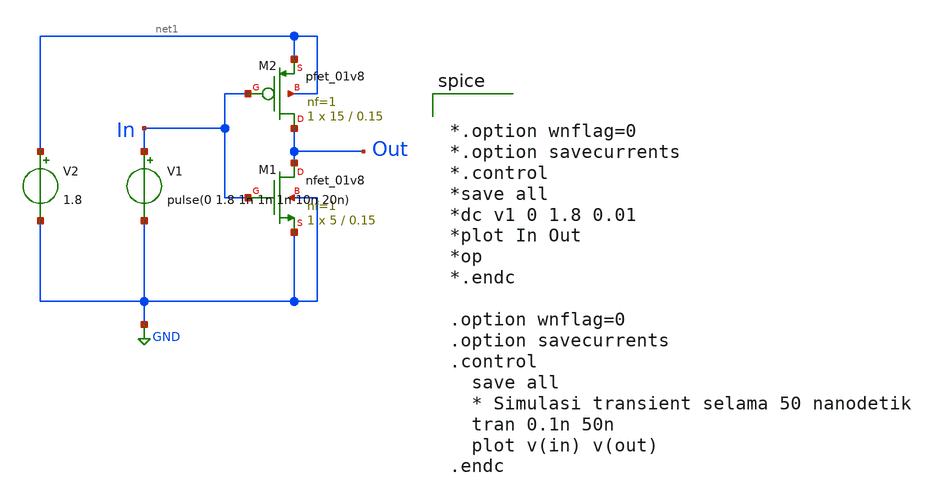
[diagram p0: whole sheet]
** sch_path: arnold_cmos_inv.sch
**.subckt arnold_cmos_inv
XM1 Out In GND GND sky130_fd_pr__nfet_01v8 L=0.15 W=5 nf=1 ad='int((1 + 1)/2) * 5 / 1 * 0.29' as='int((1 + 2)/2) * 5 / 1 * 0.29'
+ pd='2*int((1 + 1)/2) * (5 / 1 + 0.29)' ps='2*int((1 + 2)/2) * (5 / 1 + 0.29)' nrd='0.29 / 5 ' nrs='0.29 / 5 '
+ sa=0 sb=0 sd=0 mult=1 m=1
XM2 Out In net1 net1 sky130_fd_pr__pfet_01v8 L=0.15 W=15 nf=1 ad='int((1 + 1)/2) * 15 / 1 * 0.29' as='int((1 + 2)/2) * 15 / 1 * 0.29'
+ pd='2*int((1 + 1)/2) * (15 / 1 + 0.29)' ps='2*int((1 + 2)/2) * (15 / 1 + 0.29)' nrd='0.29 / 15 ' nrs='0.29 / 15 '
+ sa=0 sb=0 sd=0 mult=1 m=1
V1 In GND pulse(0 1.8 1n 1n 1n 10n 20n)
V2 net1 GND 1.8
**** begin user architecture code


.lib /foss/pdks/sky130A/libs.tech/ngspice/sky130.lib.spice tt

.param mc_mm_switch=0
.param mc_pr_switch=1




*.option wnflag=0
*.option savecurrents
*.control
*save all
*dc v1 0 1.8 0.01
*plot In Out
*op
*.endc

.option wnflag=0
.option savecurrents
.control
  save all
  * Simulasi transient selama 50 nanodetik
  tran 0.1n 50n
  plot v(in) v(out)
.endc


**** end user architecture code
**.ends
.GLOBAL GND
.end
